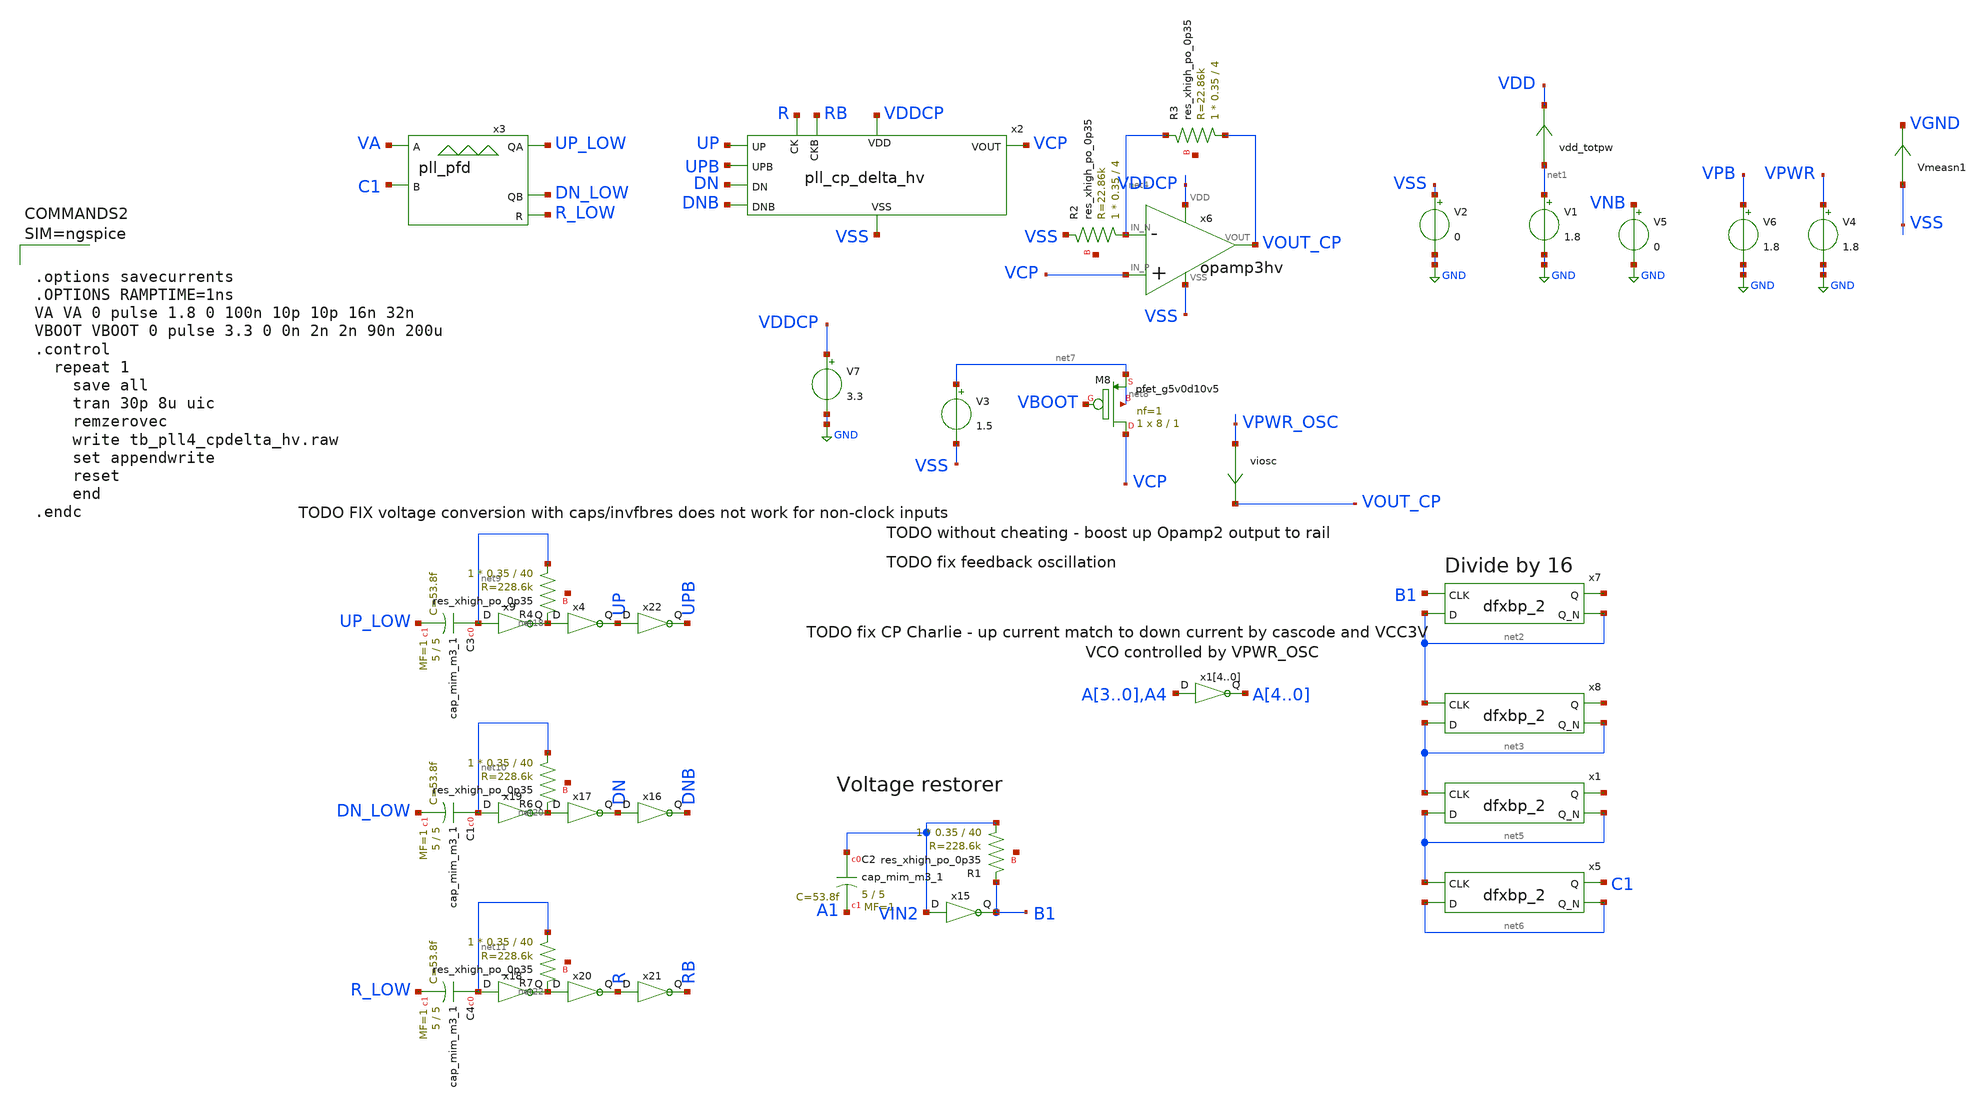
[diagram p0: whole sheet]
** sch_path: xschem/tb_pll4_cpdelta_hv.sch
**.subckt tb_pll4_cpdelta_hv
V5 VNB GND 0
V6 VPB GND 1.8
V1 net1 GND 1.8
V2 VSS GND 0
vdd_totpw net1 VDD 0
.save i(vdd_totpw)
Vmeasn1 VSS VGND 0
.save i(vmeasn1)
x3 VA C1 UP_LOW DN_LOW R_LOW VDD VSS pll_pfd
x7 B1 net2 VGND VNB VPB VPWR net12 net2 sky130_fd_sc_hd__dfxbp_2
x8 net2 net3 VGND VNB VPB VPWR net13 net3 sky130_fd_sc_hd__dfxbp_2
V4 VPWR GND 1.8
x1 net3 net5 VGND VNB VPB VPWR net14 net5 sky130_fd_sc_hd__dfxbp_2
x5 net5 net6 VGND VNB VPB VPWR C1 net6 sky130_fd_sc_hd__dfxbp_2
x14 A3 A4 VPWR_OSC VSS pll_inv1
x13 A2 A3 VPWR_OSC VSS pll_inv1
x12 A1 A2 VPWR_OSC VSS pll_inv1
x11 A0 A1 VPWR_OSC VSS pll_inv1
x10 A4 A0 VPWR_OSC VSS pll_inv1
V7 VDDCP GND 3.3
x15 VIN2 B1 VDD VSS pll_inv1
XR1 VIN2 B1 net15 sky130_fd_pr__res_xhigh_po_0p35 L=40 mult=1 m=1
XC2 VIN2 A1 sky130_fd_pr__cap_mim_m3_1 W=5 L=5 MF=1 m=1
XR2 net4 VSS net16 sky130_fd_pr__res_xhigh_po_0p35 L=4 mult=1 m=1
XR3 VOUT_CP net4 net17 sky130_fd_pr__res_xhigh_po_0p35 L=4 mult=1 m=1
viosc VPWR_OSC VOUT_CP 0
.save i(viosc)
V3 net7 VSS 1.5
XC3 net9 UP_LOW sky130_fd_pr__cap_mim_m3_1 W=5 L=5 MF=1 m=1
XR4 net9 net18 net19 sky130_fd_pr__res_xhigh_po_0p35 L=40 mult=1 m=1
XC1 net10 DN_LOW sky130_fd_pr__cap_mim_m3_1 W=5 L=5 MF=1 m=1
XR6 net10 net20 net21 sky130_fd_pr__res_xhigh_po_0p35 L=40 mult=1 m=1
XC4 net11 R_LOW sky130_fd_pr__cap_mim_m3_1 W=5 L=5 MF=1 m=1
XR7 net11 net22 net23 sky130_fd_pr__res_xhigh_po_0p35 L=40 mult=1 m=1
x22 UP UPB VSS VNB VDDCP VDDCP pll_inv2_hv
x6 VDDCP VCP net4 VOUT_CP VSS opamp3hv
XM8 VCP VBOOT net7 net8 sky130_fd_pr__pfet_g5v0d10v5 L=1 W=8 nf=1 ad='int((nf+1)/2) * W/nf * 0.29' as='int((nf+2)/2) * W/nf * 0.29'
+ pd='2*int((nf+1)/2) * (W/nf + 0.29)' ps='2*int((nf+2)/2) * (W/nf + 0.29)' nrd='0.29 / W' nrs='0.29 / W'
+ sa=0 sb=0 sd=0 mult=1 m=1
x2 VDDCP UP DN VCP VSS UPB DNB R RB pll_cp_delta_hv
x4 net18 UP VSS VNB VDDCP VDDCP pll_inv2_hv
x9 net9 net18 VSS VNB VDDCP VDDCP pll_inv2_hv
x16 DN DNB VSS VNB VDDCP VDDCP pll_inv2_hv
x17 net20 DN VSS VNB VDDCP VDDCP pll_inv2_hv
x19 net10 net20 VSS VNB VDDCP VDDCP pll_inv2_hv
x18 net11 net22 VSS VNB VDDCP VDDCP pll_inv2_hv
x20 net22 R VSS VNB VDDCP VDDCP pll_inv2_hv
x21 R RB VSS VNB VDDCP VDDCP pll_inv2_hv
**** begin user architecture code

** opencircuitdesign pdks install
.lib $::SKYWATER_MODELS/sky130.lib.spice tt_mm
.include $::SKYWATER_STDCELLS/sky130_fd_sc_hd.spice





.options savecurrents
.OPTIONS RAMPTIME=1ns
VA VA 0 pulse 1.8 0 100n 10p 10p 16n 32n
VBOOT VBOOT 0 pulse 3.3 0 0n 2n 2n 90n 200u
.control
  repeat 1
    save all
    tran 30p 8u uic
    remzerovec
    write tb_pll4_cpdelta_hv.raw
    set appendwrite
    reset
    end
.endc



**** end user architecture code
**.ends
.GLOBAL GND
.end
